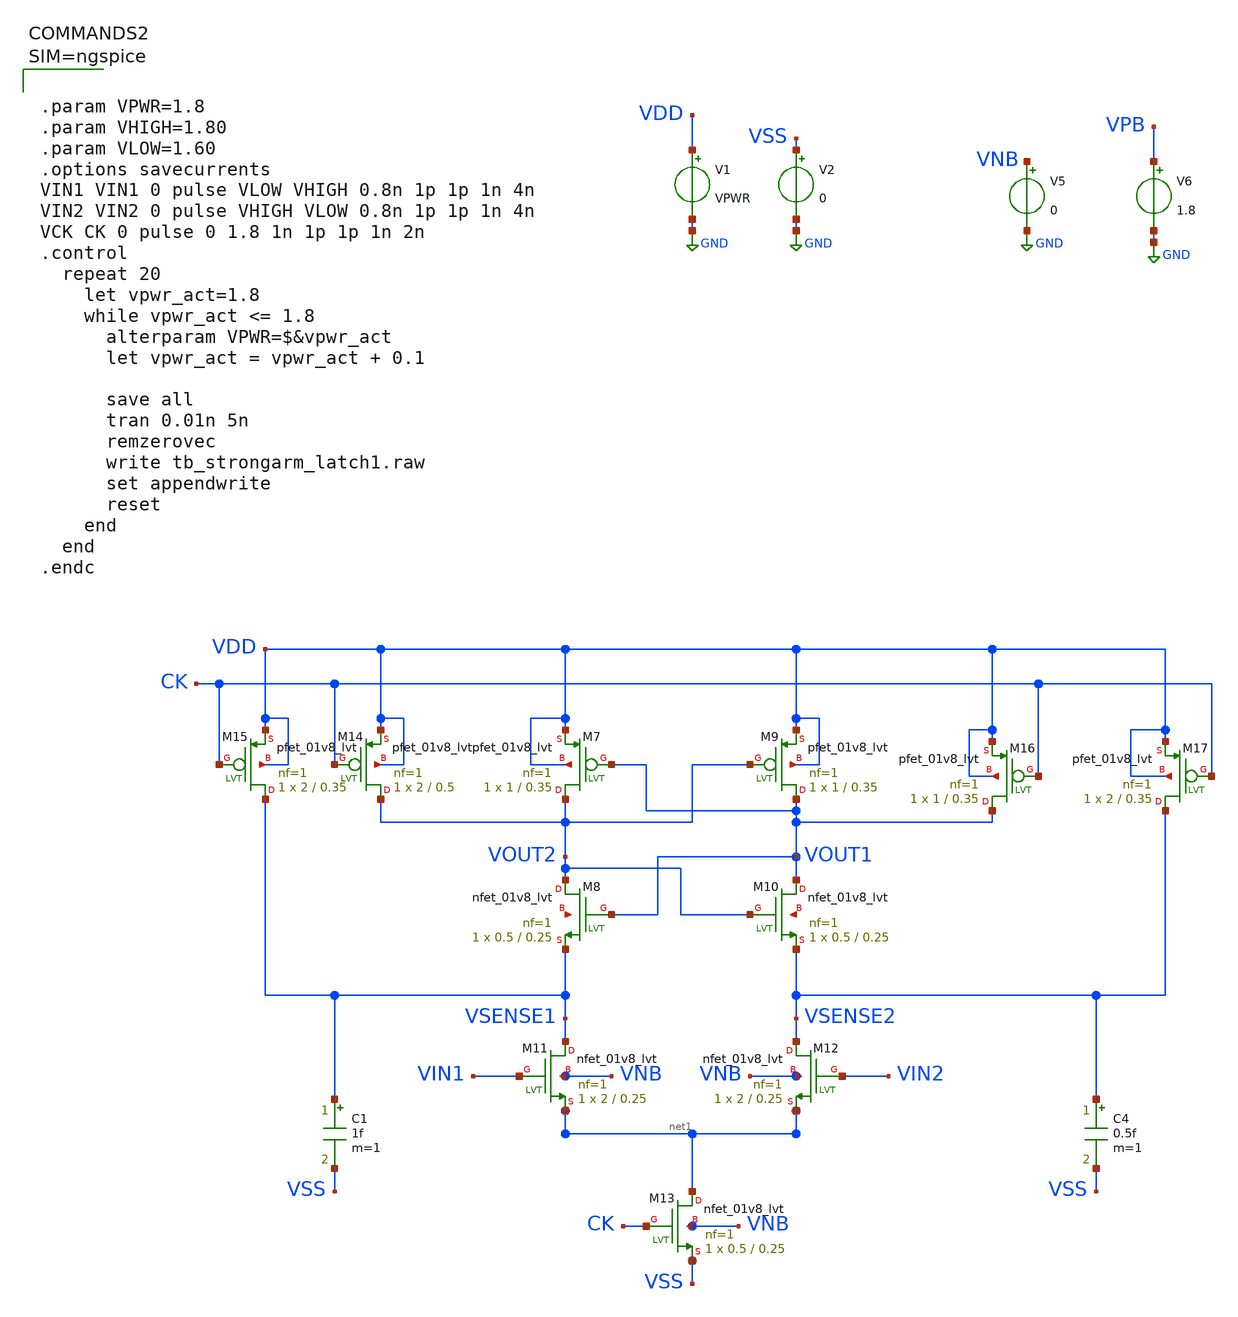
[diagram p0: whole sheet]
** sch_path: xschem/tb_strongarm_latch1.sch
**.subckt tb_strongarm_latch1
V5 VNB GND 0
V6 VPB GND 1.8
V2 VSS GND 0
V1 VDD GND VPWR
XM7 VOUT2 VOUT1 VDD VDD sky130_fd_pr__pfet_01v8_lvt L=0.35 W=1 nf=1 ad='int((nf+1)/2) * W/nf * 0.29'
+ as='int((nf+2)/2) * W/nf * 0.29' pd='2*int((nf+1)/2) * (W/nf + 0.29)' ps='2*int((nf+2)/2) * (W/nf + 0.29)'
+ nrd='0.29 / W' nrs='0.29 / W' sa=0 sb=0 sd=0 mult=1 m=1
XM8 VOUT2 VOUT1 VSENSE1 net2 sky130_fd_pr__nfet_01v8_lvt L=0.25 W=0.5 nf=1 ad='int((nf+1)/2) * W/nf * 0.29'
+ as='int((nf+2)/2) * W/nf * 0.29' pd='2*int((nf+1)/2) * (W/nf + 0.29)' ps='2*int((nf+2)/2) * (W/nf + 0.29)'
+ nrd='0.29 / W' nrs='0.29 / W' sa=0 sb=0 sd=0 mult=1 m=1
XM9 VOUT1 VOUT2 VDD VDD sky130_fd_pr__pfet_01v8_lvt L=0.35 W=1 nf=1 ad='int((nf+1)/2) * W/nf * 0.29'
+ as='int((nf+2)/2) * W/nf * 0.29' pd='2*int((nf+1)/2) * (W/nf + 0.29)' ps='2*int((nf+2)/2) * (W/nf + 0.29)'
+ nrd='0.29 / W' nrs='0.29 / W' sa=0 sb=0 sd=0 mult=1 m=1
XM10 VOUT1 VOUT2 VSENSE2 net3 sky130_fd_pr__nfet_01v8_lvt L=0.25 W=0.5 nf=1 ad='int((nf+1)/2) * W/nf * 0.29'
+ as='int((nf+2)/2) * W/nf * 0.29' pd='2*int((nf+1)/2) * (W/nf + 0.29)' ps='2*int((nf+2)/2) * (W/nf + 0.29)'
+ nrd='0.29 / W' nrs='0.29 / W' sa=0 sb=0 sd=0 mult=1 m=1
XM11 VSENSE1 VIN1 net1 VNB sky130_fd_pr__nfet_01v8_lvt L=0.25 W=2 nf=1 ad='int((nf+1)/2) * W/nf * 0.29'
+ as='int((nf+2)/2) * W/nf * 0.29' pd='2*int((nf+1)/2) * (W/nf + 0.29)' ps='2*int((nf+2)/2) * (W/nf + 0.29)'
+ nrd='0.29 / W' nrs='0.29 / W' sa=0 sb=0 sd=0 mult=1 m=1
XM12 VSENSE2 VIN2 net1 VNB sky130_fd_pr__nfet_01v8_lvt L=0.25 W=2 nf=1 ad='int((nf+1)/2) * W/nf * 0.29'
+ as='int((nf+2)/2) * W/nf * 0.29' pd='2*int((nf+1)/2) * (W/nf + 0.29)' ps='2*int((nf+2)/2) * (W/nf + 0.29)'
+ nrd='0.29 / W' nrs='0.29 / W' sa=0 sb=0 sd=0 mult=1 m=1
XM13 net1 CK VSS VNB sky130_fd_pr__nfet_01v8_lvt L=0.25 W=0.5 nf=1 ad='int((nf+1)/2) * W/nf * 0.29' as='int((nf+2)/2) * W/nf * 0.29'
+ pd='2*int((nf+1)/2) * (W/nf + 0.29)' ps='2*int((nf+2)/2) * (W/nf + 0.29)' nrd='0.29 / W' nrs='0.29 / W'
+ sa=0 sb=0 sd=0 mult=1 m=1
XM14 VOUT2 CK VDD VDD sky130_fd_pr__pfet_01v8_lvt L=0.5 W=2 nf=1 ad='int((nf+1)/2) * W/nf * 0.29' as='int((nf+2)/2) * W/nf * 0.29'
+ pd='2*int((nf+1)/2) * (W/nf + 0.29)' ps='2*int((nf+2)/2) * (W/nf + 0.29)' nrd='0.29 / W' nrs='0.29 / W'
+ sa=0 sb=0 sd=0 mult=1 m=1
XM15 VSENSE1 CK VDD VDD sky130_fd_pr__pfet_01v8_lvt L=0.35 W=2 nf=1 ad='int((nf+1)/2) * W/nf * 0.29'
+ as='int((nf+2)/2) * W/nf * 0.29' pd='2*int((nf+1)/2) * (W/nf + 0.29)' ps='2*int((nf+2)/2) * (W/nf + 0.29)'
+ nrd='0.29 / W' nrs='0.29 / W' sa=0 sb=0 sd=0 mult=1 m=1
XM16 VOUT1 CK VDD VDD sky130_fd_pr__pfet_01v8_lvt L=0.35 W=1 nf=1 ad='int((nf+1)/2) * W/nf * 0.29' as='int((nf+2)/2) * W/nf * 0.29'
+ pd='2*int((nf+1)/2) * (W/nf + 0.29)' ps='2*int((nf+2)/2) * (W/nf + 0.29)' nrd='0.29 / W' nrs='0.29 / W'
+ sa=0 sb=0 sd=0 mult=1 m=1
XM17 VSENSE2 CK VDD VDD sky130_fd_pr__pfet_01v8_lvt L=0.35 W=2 nf=1 ad='int((nf+1)/2) * W/nf * 0.29'
+ as='int((nf+2)/2) * W/nf * 0.29' pd='2*int((nf+1)/2) * (W/nf + 0.29)' ps='2*int((nf+2)/2) * (W/nf + 0.29)'
+ nrd='0.29 / W' nrs='0.29 / W' sa=0 sb=0 sd=0 mult=1 m=1
C4 VSENSE2 VSS 0.5f m=1
C1 VSENSE1 VSS 1f m=1
**** begin user architecture code

** opencircuitdesign pdks install
.lib $::SKYWATER_MODELS/sky130.lib.spice tt_mm
*.lib $::SKYWATER_STDCELLS/sky130_fd_sc_hd_blablabla.spice

.subckt sky130_fd_sc_hd__inv_1 A VGND VNB VPB VPWR Y
X0 VGND A Y VNB sky130_fd_pr__nfet_01v8 w=650000u l=150000u
X1 VPWR A Y VPB sky130_fd_pr__pfet_01v8_hvt w=1e+06u l=150000u
.ends





.param VPWR=1.8
.param VHIGH=1.80
.param VLOW=1.60
.options savecurrents
VIN1 VIN1 0 pulse VLOW VHIGH 0.8n 1p 1p 1n 4n
VIN2 VIN2 0 pulse VHIGH VLOW 0.8n 1p 1p 1n 4n
VCK CK 0 pulse 0 1.8 1n 1p 1p 1n 2n
.control
  repeat 20
    let vpwr_act=1.8
    while vpwr_act <= 1.8
      alterparam VPWR=$&vpwr_act
      let vpwr_act = vpwr_act + 0.1

      save all
      tran 0.01n 5n
      remzerovec
      write tb_strongarm_latch1.raw
      set appendwrite
      reset
    end
  end
.endc



**** end user architecture code
**.ends
.GLOBAL GND
.end
